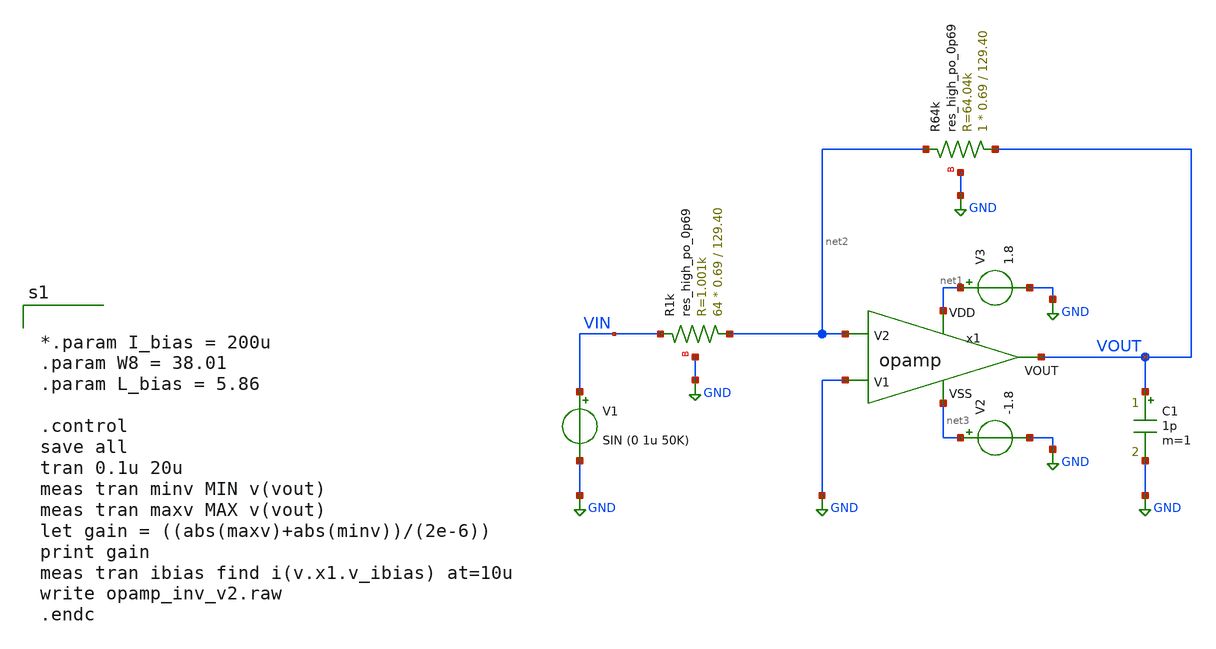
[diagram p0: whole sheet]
** sch_path: xschem/opamp_inv_v2.sch
**.subckt opamp_inv_v2
V1 VIN GND SIN (0 1u 50K)
V2 net3 GND -1.8
V3 net1 GND 1.8
x1 net1 net3 GND net2 VOUT opamp
C1 VOUT GND 1p m=1
XR1k net2 VIN GND sky130_fd_pr__res_high_po_0p69 L=129.40 mult=64 m=64
XR64k VOUT net2 GND sky130_fd_pr__res_high_po_0p69 L=129.40 mult=1 m=1
**** begin user architecture code


*.param I_bias = 200u
.param W8 = 38.01
.param L_bias = 5.86

.control
save all
tran 0.1u 20u
meas tran minv MIN v(vout)
meas tran maxv MAX v(vout)
let gain = ((abs(maxv)+abs(minv))/(2e-6))
print gain
meas tran ibias find i(v.x1.v_ibias) at=10u
write opamp_inv_v2.raw
.endc


** opencircuitdesign pdks install
.lib $::SKYWATER_MODELS/sky130.lib.spice tt


**** end user architecture code
**.ends

* expanding   symbol:  ../xschem/opamp.sym # of pins=5
** sym_path: ../xschem/opamp.sym
** sch_path: ../xschem/opamp.sch
.subckt opamp VDD VSS V1 V2 VOUT
*.ipin VSS
*.ipin VDD
*.ipin V2
*.ipin V1
*.opin VOUT
XM2 net5 V2 net1 VSS sky130_fd_pr__nfet_g5v0d10v5 L=1 W=18 nf=1 ad='int((nf+1)/2) * W/nf * 0.29' as='int((nf+2)/2) * W/nf * 0.29'
+ pd='2*int((nf+1)/2) * (W/nf + 0.29)' ps='2*int((nf+2)/2) * (W/nf + 0.29)' nrd='0.29 / W' nrs='0.29 / W'
+ sa=0 sb=0 sd=0 mult=1 m=1
XM1 net6 net5 VDD VDD sky130_fd_pr__pfet_g5v0d10v5 L=1 W=30 nf=1 ad='int((nf+1)/2) * W/nf * 0.29' as='int((nf+2)/2) * W/nf * 0.29'
+ pd='2*int((nf+1)/2) * (W/nf + 0.29)' ps='2*int((nf+2)/2) * (W/nf + 0.29)' nrd='0.29 / W' nrs='0.29 / W'
+ sa=0 sb=0 sd=0 mult=1 m=1
XM4 net6 V1 net1 VSS sky130_fd_pr__nfet_g5v0d10v5 L=1 W=18 nf=1 ad='int((nf+1)/2) * W/nf * 0.29' as='int((nf+2)/2) * W/nf * 0.29'
+ pd='2*int((nf+1)/2) * (W/nf + 0.29)' ps='2*int((nf+2)/2) * (W/nf + 0.29)' nrd='0.29 / W' nrs='0.29 / W'
+ sa=0 sb=0 sd=0 mult=1 m=1
XM5 net1 net4 VSS VSS sky130_fd_pr__nfet_g5v0d10v5 L=1 W=15.171 nf=1 ad='int((nf+1)/2) * W/nf * 0.29'
+ as='int((nf+2)/2) * W/nf * 0.29' pd='2*int((nf+1)/2) * (W/nf + 0.29)' ps='2*int((nf+2)/2) * (W/nf + 0.29)'
+ nrd='0.29 / W' nrs='0.29 / W' sa=0 sb=0 sd=0 mult=1 m=1
XM6 VOUT net4 VSS VSS sky130_fd_pr__nfet_g5v0d10v5 L=1 W=19 nf=1 ad='int((nf+1)/2) * W/nf * 0.29' as='int((nf+2)/2) * W/nf * 0.29'
+ pd='2*int((nf+1)/2) * (W/nf + 0.29)' ps='2*int((nf+2)/2) * (W/nf + 0.29)' nrd='0.29 / W' nrs='0.29 / W'
+ sa=0 sb=0 sd=0 mult=1 m=1
XM7 net4 net4 VSS VSS sky130_fd_pr__nfet_g5v0d10v5 L=1 W=20 nf=1 ad='int((nf+1)/2) * W/nf * 0.29' as='int((nf+2)/2) * W/nf * 0.29'
+ pd='2*int((nf+1)/2) * (W/nf + 0.29)' ps='2*int((nf+2)/2) * (W/nf + 0.29)' nrd='0.29 / W' nrs='0.29 / W'
+ sa=0 sb=0 sd=0 mult=1 m=1
XM3 net5 net5 VDD VDD sky130_fd_pr__pfet_g5v0d10v5 L=1 W=30 nf=1 ad='int((nf+1)/2) * W/nf * 0.29' as='int((nf+2)/2) * W/nf * 0.29'
+ pd='2*int((nf+1)/2) * (W/nf + 0.29)' ps='2*int((nf+2)/2) * (W/nf + 0.29)' nrd='0.29 / W' nrs='0.29 / W'
+ sa=0 sb=0 sd=0 mult=1 m=1
XM8 VOUT net6 VDD VDD sky130_fd_pr__pfet_g5v0d10v5 L=1 W=38 nf=1 ad='int((nf+1)/2) * W/nf * 0.29' as='int((nf+2)/2) * W/nf * 0.29'
+ pd='2*int((nf+1)/2) * (W/nf + 0.29)' ps='2*int((nf+2)/2) * (W/nf + 0.29)' nrd='0.29 / W' nrs='0.29 / W'
+ sa=0 sb=0 sd=0 mult=2 m=2
XR3 net2 VDD VSS sky130_fd_pr__res_high_po W=1 L=30 mult=1 m=1
XR1 net3 net2 VSS sky130_fd_pr__res_high_po W=1 L=30 mult=1 m=1
XR2 net4 net3 VSS sky130_fd_pr__res_high_po W=1 L=30 mult=1 m=1
XR4 net7 VOUT VSS sky130_fd_pr__res_high_po W=1 L=5 mult=1 m=1
XC1 net7 net6 sky130_fd_pr__cap_mim_m3_1 W=5.5 L=10 MF=10 m=10
.ends

.GLOBAL GND
.end
